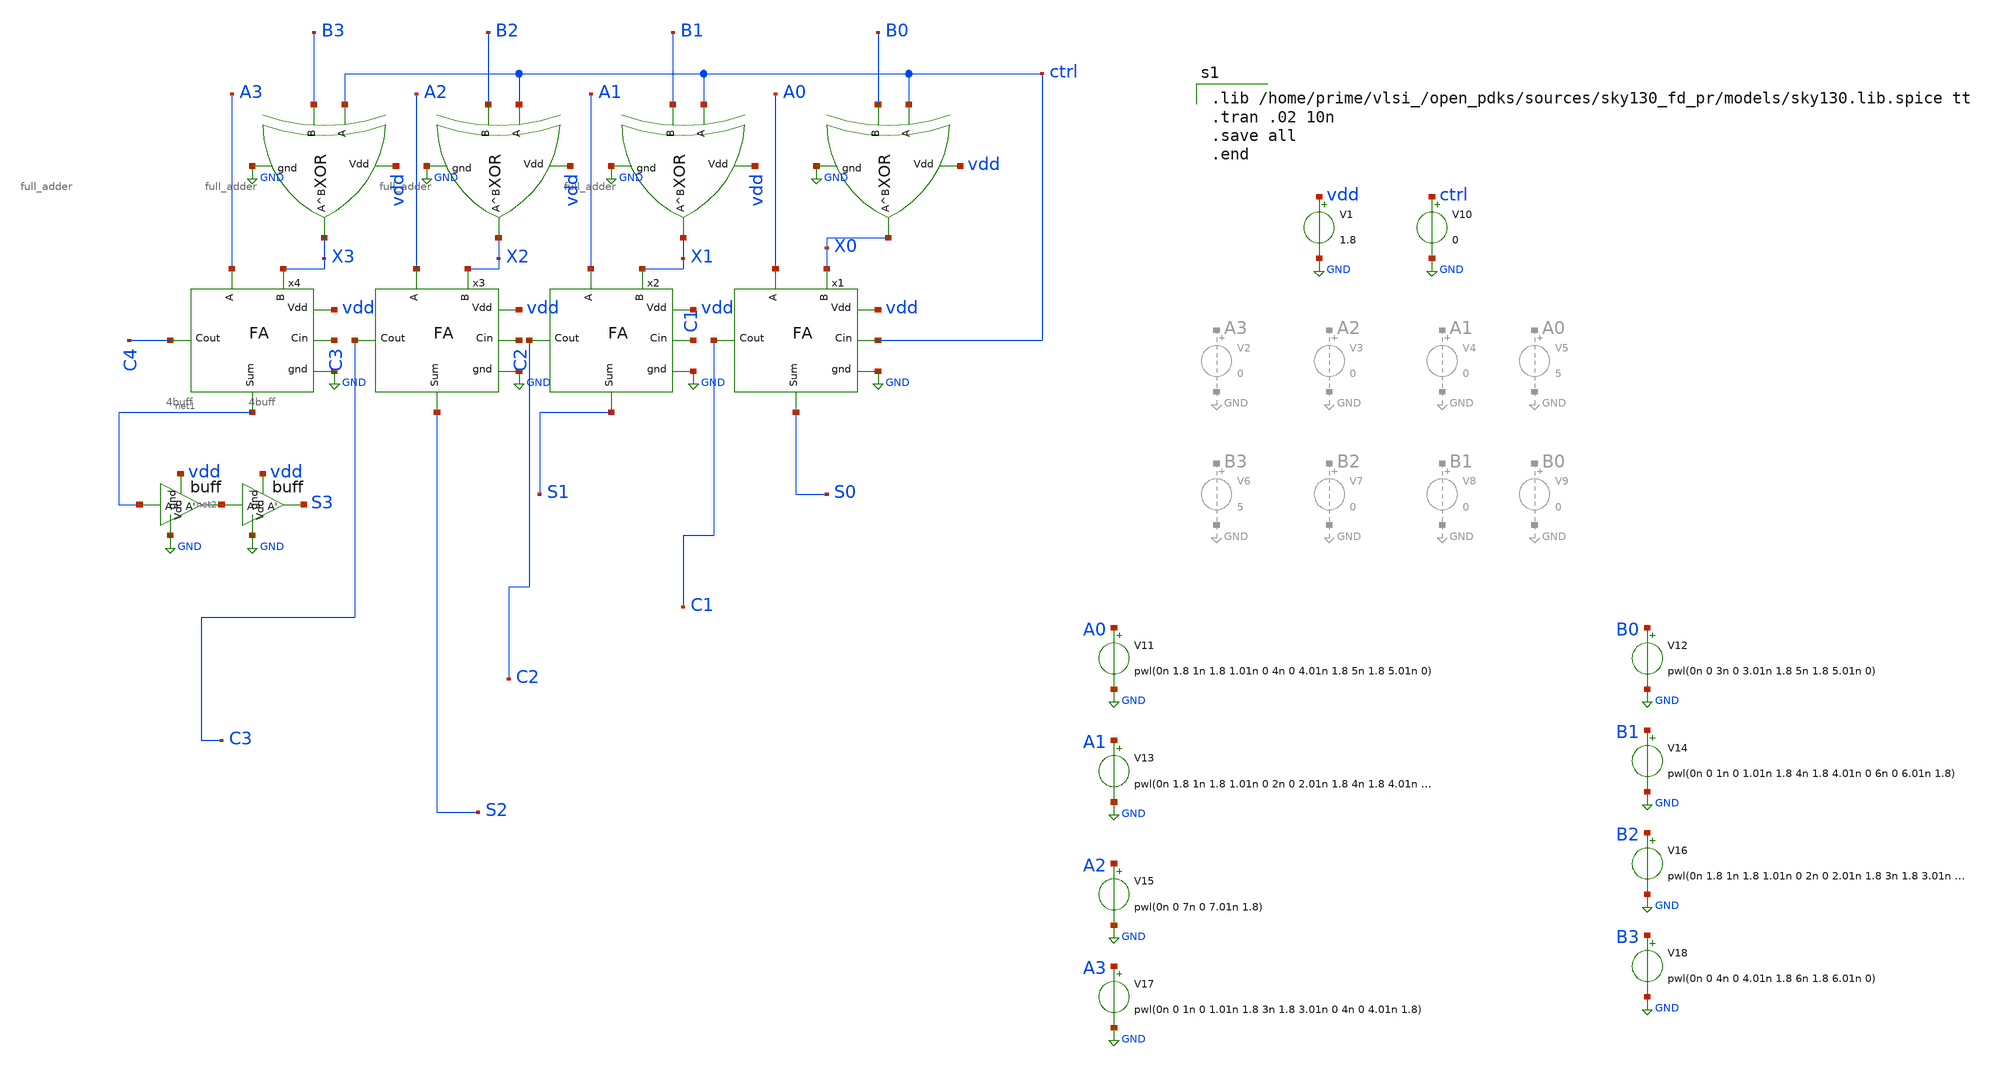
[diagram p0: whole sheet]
** sch_path: extra_stuff/adder_subtractor.sch
**.subckt adder_subtractor
x1 S0 C1 ctrl vdd GND A0 X0 full_adder
x2 S1 C2 C1 vdd GND A1 X1 full_adder
x3 S2 C3 C2 vdd GND A2 X2 full_adder
x4 net1 C4 C3 vdd GND A3 X3 full_adder
x5 vdd GND X0 ctrl B0 xor
x6 vdd GND X1 ctrl B1 xor
x7 vdd GND X2 ctrl B2 xor
x8 vdd GND X3 ctrl B3 xor
V1 vdd GND 1.8
V10 ctrl GND 0
V11 A0 GND pwl(0n 1.8 1n 1.8 1.01n 0 4n 0 4.01n 1.8 5n 1.8 5.01n 0)
V12 B0 GND pwl(0n 0 3n 0 3.01n 1.8 5n 1.8 5.01n 0)
V13 A1 GND pwl(0n 1.8 1n 1.8 1.01n 0 2n 0 2.01n 1.8 4n 1.8 4.01n 0 6n 0 6.01n 1.8 7n 1.8 7.01n 0)
V14 B1 GND pwl(0n 0 1n 0 1.01n 1.8 4n 1.8 4.01n 0 6n 0 6.01n 1.8)
V15 A2 GND pwl(0n 0 7n 0 7.01n 1.8)
V16 B2 GND pwl(0n 1.8 1n 1.8 1.01n 0 2n 0 2.01n 1.8 3n 1.8 3.01n 0 4n 0 4.01n 1.8 5n 1.8 5.01n 0 6n
+ 0 6.01n 1.8)
V17 A3 GND pwl(0n 0 1n 0 1.01n 1.8 3n 1.8 3.01n 0 4n 0 4.01n 1.8)
V18 B3 GND pwl(0n 0 4n 0 4.01n 1.8 6n 1.8 6.01n 0)
x19 net2 GND net1 vdd 4buff
x20 S3 GND net2 vdd 4buff
**** begin user architecture code

.lib /home/prime/vlsi_/open_pdks/sources/sky130_fd_pr/models/sky130.lib.spice tt
.tran .02 10n
.save all
.end

**** end user architecture code
**.ends
.GLOBAL GND
.end
